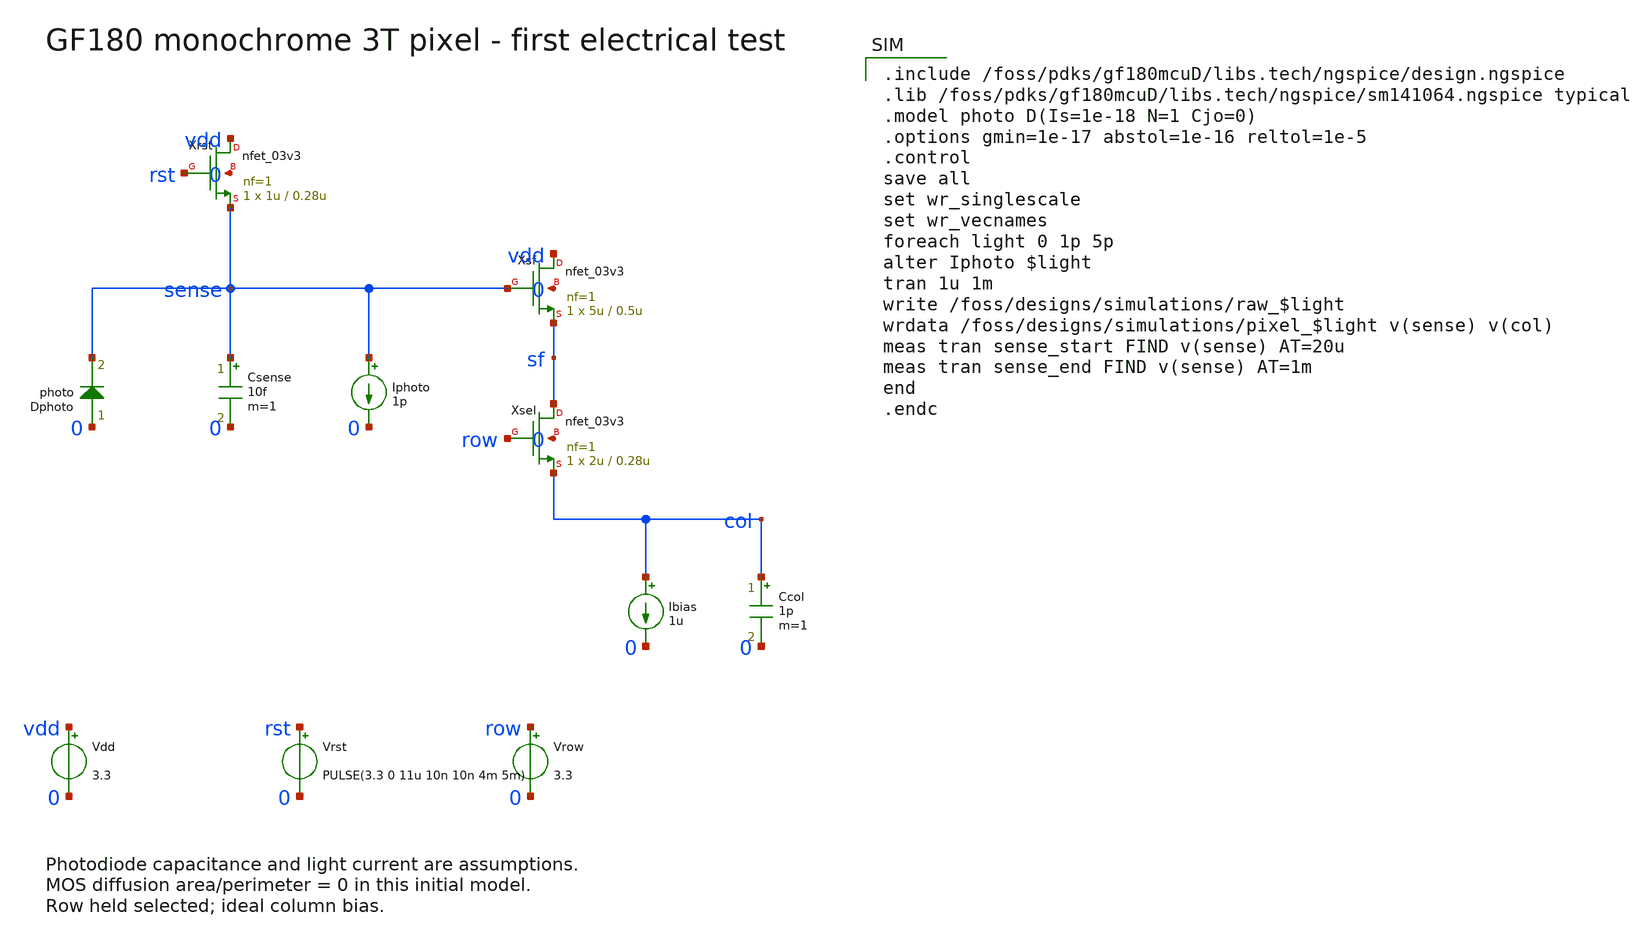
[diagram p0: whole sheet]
** sch_path: xschem/pixel_3t.sch
**.subckt pixel_3t
Xrst vdd rst sense 0 nfet_03v3 L=0.28u W=1u nf=1 ad=0 as=0 pd=0 ps=0 nrd=0 nrs=0 sa=0 sb=0 sd=0 m=1
Xsf vdd sense sf 0 nfet_03v3 L=0.5u W=5u nf=1 ad=0 as=0 pd=0 ps=0 nrd=0 nrs=0 sa=0 sb=0 sd=0 m=1
Xsel sf row col 0 nfet_03v3 L=0.28u W=2u nf=1 ad=0 as=0 pd=0 ps=0 nrd=0 nrs=0 sa=0 sb=0 sd=0 m=1
Dphoto 0 sense photo area=1
Csense sense 0 10f m=1
Iphoto sense 0 1p
Ibias col 0 1u
Ccol col 0 1p m=1
Vdd vdd 0 3.3
Vrst rst 0 PULSE(3.3 0 11u 10n 10n 4m 5m)
Vrow row 0 3.3
**** begin user architecture code

.include /foss/pdks/gf180mcuD/libs.tech/ngspice/design.ngspice
.lib /foss/pdks/gf180mcuD/libs.tech/ngspice/sm141064.ngspice typical
.model photo D(Is=1e-18 N=1 Cjo=0)
.options gmin=1e-17 abstol=1e-16 reltol=1e-5
.control
save all
set wr_singlescale
set wr_vecnames
foreach light 0 1p 5p
alter Iphoto $light
tran 1u 1m
write /foss/designs/simulations/raw_$light
wrdata /foss/designs/simulations/pixel_$light v(sense) v(col)
meas tran sense_start FIND v(sense) AT=20u
meas tran sense_end FIND v(sense) AT=1m
end
.endc

**** end user architecture code
**.ends
.end
